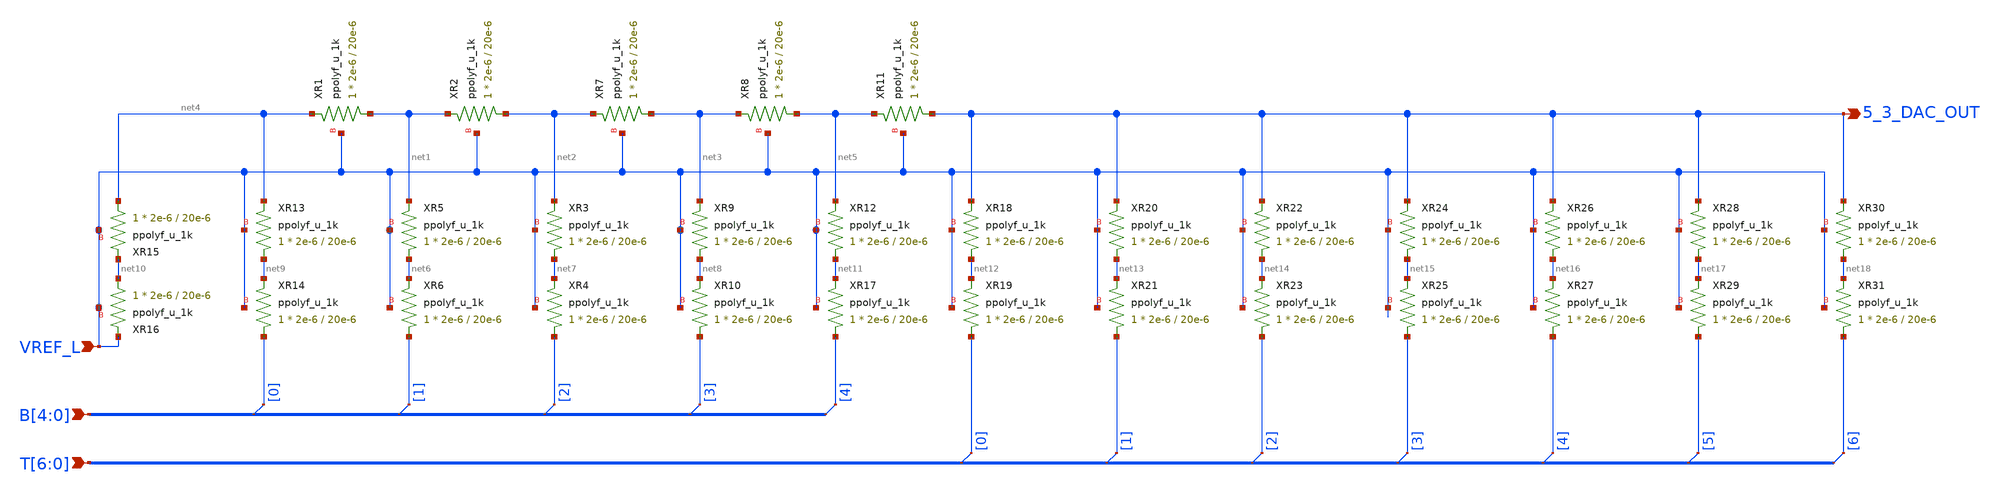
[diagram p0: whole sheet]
** sch_path: xschem/5_3_dac.sch
**.subckt 5_3_dac 5_3_DAC_OUT VREF_L B[4],B[3],B[2],B[1],B[0] T[6],T[5],T[4],T[3],T[2],T[1],T[0]
*.opin 5_3_DAC_OUT
*.ipin VREF_L
*.ipin B[4],B[3],B[2],B[1],B[0]
*.ipin T[6],T[5],T[4],T[3],T[2],T[1],T[0]
XR1 net1 net4 VREF_L ppolyf_u_1k r_width=2e-6 r_length=20e-6 m=1
XR2 net2 net1 VREF_L ppolyf_u_1k r_width=2e-6 r_length=20e-6 m=1
XR5 net6 net1 VREF_L ppolyf_u_1k r_width=2e-6 r_length=20e-6 m=1
XR6 B[1] net6 VREF_L ppolyf_u_1k r_width=2e-6 r_length=20e-6 m=1
XR3 net7 net2 VREF_L ppolyf_u_1k r_width=2e-6 r_length=20e-6 m=1
XR4 B[2] net7 VREF_L ppolyf_u_1k r_width=2e-6 r_length=20e-6 m=1
XR7 net3 net2 VREF_L ppolyf_u_1k r_width=2e-6 r_length=20e-6 m=1
XR8 net5 net3 VREF_L ppolyf_u_1k r_width=2e-6 r_length=20e-6 m=1
XR9 net8 net3 VREF_L ppolyf_u_1k r_width=2e-6 r_length=20e-6 m=1
XR10 B[3] net8 VREF_L ppolyf_u_1k r_width=2e-6 r_length=20e-6 m=1
XR13 net9 net4 VREF_L ppolyf_u_1k r_width=2e-6 r_length=20e-6 m=1
XR14 B[0] net9 VREF_L ppolyf_u_1k r_width=2e-6 r_length=20e-6 m=1
XR15 net4 net10 VREF_L ppolyf_u_1k r_width=2e-6 r_length=20e-6 m=1
XR16 net10 VREF_L VREF_L ppolyf_u_1k r_width=2e-6 r_length=20e-6 m=1
XR11 5_3_DAC_OUT net5 VREF_L ppolyf_u_1k r_width=2e-6 r_length=20e-6 m=1
XR12 net11 net5 VREF_L ppolyf_u_1k r_width=2e-6 r_length=20e-6 m=1
XR17 B[4] net11 VREF_L ppolyf_u_1k r_width=2e-6 r_length=20e-6 m=1
* tap: B[4:0] --> B[0]
* tap: B[4:0] --> B[1]
* tap: B[4:0] --> B[2]
* tap: B[4:0] --> B[3]
* tap: B[4:0] --> B[4]
XR18 net12 5_3_DAC_OUT VREF_L ppolyf_u_1k r_width=2e-6 r_length=20e-6 m=1
XR19 T[0] net12 VREF_L ppolyf_u_1k r_width=2e-6 r_length=20e-6 m=1
XR20 net13 5_3_DAC_OUT VREF_L ppolyf_u_1k r_width=2e-6 r_length=20e-6 m=1
XR21 T[1] net13 VREF_L ppolyf_u_1k r_width=2e-6 r_length=20e-6 m=1
XR22 net14 5_3_DAC_OUT VREF_L ppolyf_u_1k r_width=2e-6 r_length=20e-6 m=1
XR23 T[2] net14 VREF_L ppolyf_u_1k r_width=2e-6 r_length=20e-6 m=1
XR24 net15 5_3_DAC_OUT VREF_L ppolyf_u_1k r_width=2e-6 r_length=20e-6 m=1
XR25 T[3] net15 VREF_L ppolyf_u_1k r_width=2e-6 r_length=20e-6 m=1
XR26 net16 5_3_DAC_OUT VREF_L ppolyf_u_1k r_width=2e-6 r_length=20e-6 m=1
XR27 T[4] net16 VREF_L ppolyf_u_1k r_width=2e-6 r_length=20e-6 m=1
XR28 net17 5_3_DAC_OUT VREF_L ppolyf_u_1k r_width=2e-6 r_length=20e-6 m=1
XR29 T[5] net17 VREF_L ppolyf_u_1k r_width=2e-6 r_length=20e-6 m=1
XR30 net18 5_3_DAC_OUT VREF_L ppolyf_u_1k r_width=2e-6 r_length=20e-6 m=1
XR31 T[6] net18 VREF_L ppolyf_u_1k r_width=2e-6 r_length=20e-6 m=1
* tap: T[6:0] --> T[0]
* tap: T[6:0] --> T[1]
* tap: T[6:0] --> T[2]
* tap: T[6:0] --> T[3]
* tap: T[6:0] --> T[4]
* tap: T[6:0] --> T[5]
* tap: T[6:0] --> T[6]
**.ends
.end
